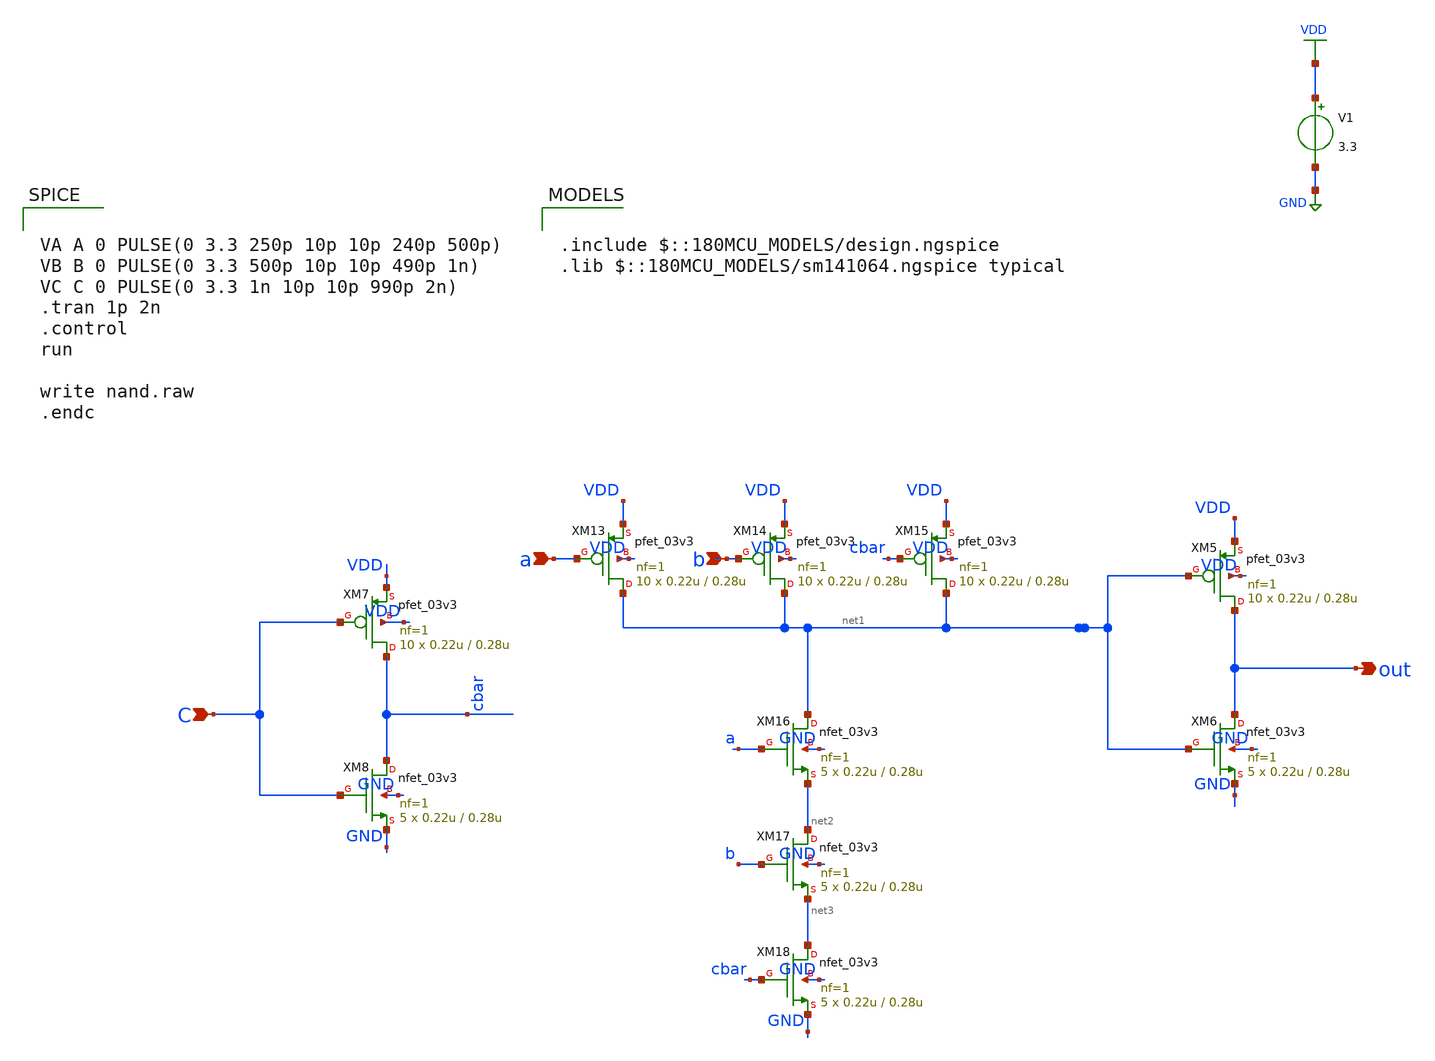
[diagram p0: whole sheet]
** sch_path: blocks/adc/encoder/tb/NAND3_tb.sch
**.subckt NAND3_tb a out C b
*.ipin a
*.opin out
*.ipin C
*.ipin b
V1 VDD GND 3.3
XM5 out net1 VDD VDD pfet_03v3 L=0.28u W=0.22u nf=1 ad='int((nf+1)/2) * W/nf * 0.18u' as='int((nf+2)/2) * W/nf * 0.18u'
+ pd='2*int((nf+1)/2) * (W/nf + 0.18u)' ps='2*int((nf+2)/2) * (W/nf + 0.18u)' nrd='0.18u / W' nrs='0.18u / W'
+ sa=0 sb=0 sd=0 m=10
XM6 out net1 GND GND nfet_03v3 L=0.28u W=0.22u nf=1 ad='int((nf+1)/2) * W/nf * 0.18u' as='int((nf+2)/2) * W/nf * 0.18u'
+ pd='2*int((nf+1)/2) * (W/nf + 0.18u)' ps='2*int((nf+2)/2) * (W/nf + 0.18u)' nrd='0.18u / W' nrs='0.18u / W'
+ sa=0 sb=0 sd=0 m=5
XM7 cbar C VDD VDD pfet_03v3 L=0.28u W=0.22u nf=1 ad='int((nf+1)/2) * W/nf * 0.18u' as='int((nf+2)/2) * W/nf * 0.18u'
+ pd='2*int((nf+1)/2) * (W/nf + 0.18u)' ps='2*int((nf+2)/2) * (W/nf + 0.18u)' nrd='0.18u / W' nrs='0.18u / W'
+ sa=0 sb=0 sd=0 m=10
XM8 cbar C GND GND nfet_03v3 L=0.28u W=0.22u nf=1 ad='int((nf+1)/2) * W/nf * 0.18u' as='int((nf+2)/2) * W/nf * 0.18u'
+ pd='2*int((nf+1)/2) * (W/nf + 0.18u)' ps='2*int((nf+2)/2) * (W/nf + 0.18u)' nrd='0.18u / W' nrs='0.18u / W'
+ sa=0 sb=0 sd=0 m=5
XM13 net1 a VDD VDD pfet_03v3 L=0.28u W=0.22u nf=1 ad='int((nf+1)/2) * W/nf * 0.18u' as='int((nf+2)/2) * W/nf * 0.18u'
+ pd='2*int((nf+1)/2) * (W/nf + 0.18u)' ps='2*int((nf+2)/2) * (W/nf + 0.18u)' nrd='0.18u / W' nrs='0.18u / W'
+ sa=0 sb=0 sd=0 m=10
XM14 net1 b VDD VDD pfet_03v3 L=0.28u W=0.22u nf=1 ad='int((nf+1)/2) * W/nf * 0.18u' as='int((nf+2)/2) * W/nf * 0.18u'
+ pd='2*int((nf+1)/2) * (W/nf + 0.18u)' ps='2*int((nf+2)/2) * (W/nf + 0.18u)' nrd='0.18u / W' nrs='0.18u / W'
+ sa=0 sb=0 sd=0 m=10
XM15 net1 cbar VDD VDD pfet_03v3 L=0.28u W=0.22u nf=1 ad='int((nf+1)/2) * W/nf * 0.18u' as='int((nf+2)/2) * W/nf * 0.18u'
+ pd='2*int((nf+1)/2) * (W/nf + 0.18u)' ps='2*int((nf+2)/2) * (W/nf + 0.18u)' nrd='0.18u / W' nrs='0.18u / W'
+ sa=0 sb=0 sd=0 m=10
XM16 net1 a net2 GND nfet_03v3 L=0.28u W=0.22u nf=1 ad='int((nf+1)/2) * W/nf * 0.18u' as='int((nf+2)/2) * W/nf * 0.18u'
+ pd='2*int((nf+1)/2) * (W/nf + 0.18u)' ps='2*int((nf+2)/2) * (W/nf + 0.18u)' nrd='0.18u / W' nrs='0.18u / W'
+ sa=0 sb=0 sd=0 m=5
XM17 net2 b net3 GND nfet_03v3 L=0.28u W=0.22u nf=1 ad='int((nf+1)/2) * W/nf * 0.18u' as='int((nf+2)/2) * W/nf * 0.18u'
+ pd='2*int((nf+1)/2) * (W/nf + 0.18u)' ps='2*int((nf+2)/2) * (W/nf + 0.18u)' nrd='0.18u / W' nrs='0.18u / W'
+ sa=0 sb=0 sd=0 m=5
XM18 net3 cbar GND GND nfet_03v3 L=0.28u W=0.22u nf=1 ad='int((nf+1)/2) * W/nf * 0.18u' as='int((nf+2)/2) * W/nf * 0.18u'
+ pd='2*int((nf+1)/2) * (W/nf + 0.18u)' ps='2*int((nf+2)/2) * (W/nf + 0.18u)' nrd='0.18u / W' nrs='0.18u / W'
+ sa=0 sb=0 sd=0 m=5
**** begin user architecture code


VA A 0 PULSE(0 3.3 250p 10p 10p 240p 500p)
VB B 0 PULSE(0 3.3 500p 10p 10p 490p 1n)
VC C 0 PULSE(0 3.3 1n 10p 10p 990p 2n)
.tran 1p 2n
.control
run

write nand.raw
.endc



.include $::180MCU_MODELS/design.ngspice
.lib $::180MCU_MODELS/sm141064.ngspice typical

**** end user architecture code
**.ends
.GLOBAL VDD
.GLOBAL GND
.end
